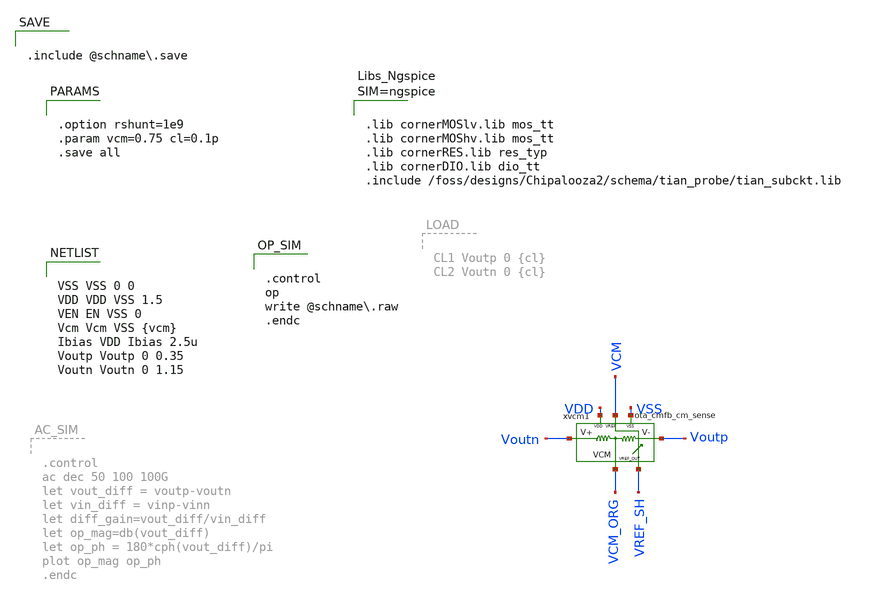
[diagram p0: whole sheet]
** sch_path: schema/ota_cmfb_cm_sense/ota_cmfb_cm_sense_tb.sch
**.subckt ota_cmfb_cm_sense_tb
xvcm1 Voutn Voutp VCM_ORG VDD VSS VREF_SH VCM ota_cmfb_cm_sense
**** begin user architecture code


VSS VSS 0 0
VDD VDD VSS 1.5
VEN EN VSS 0
Vcm Vcm VSS {vcm}
Ibias VDD Ibias 2.5u
Voutp Voutp 0 0.35
Voutn Voutn 0 1.15




.control
op
write @schname\.raw
.endc





.lib cornerMOSlv.lib mos_tt
.lib cornerMOShv.lib mos_tt
.lib cornerRES.lib res_typ
.lib cornerDIO.lib dio_tt
.include /foss/designs/Chipalooza2/schema/tian_probe/tian_subckt.lib





.option rshunt=1e9
.param vcm=0.75 cl=0.1p
.save all



.include @schname.save

**** end user architecture code
**.ends

* expanding   symbol:  /foss/designs/Chipalooza2/schema/ota_cmfb_cm_sense/ota_cmfb_cm_sense.sym # of
*+ pins=7
** sym_path: schema/ota_cmfb_cm_sense/ota_cmfb_cm_sense.sym
** sch_path: schema/ota_cmfb_cm_sense/ota_cmfb_cm_sense.sch
.subckt ota_cmfb_cm_sense Voutp Voutn VCM VDD VSS VREF_OUT VREF
*.ipin Voutp
*.ipin Voutn
*.opin VCM
*.iopin VDD
*.iopin VSS
*.ipin VREF
*.opin VREF_OUT
XR1 Voutn VCM VSS rhigh w=0.5e-6 l=1e-6*20 m=1 b=0 mm_ok=1
XR2 Voutp VCM VSS rhigh w=0.5e-6 l=1e-6*20 m=1 b=0 mm_ok=1
.ends

.end
